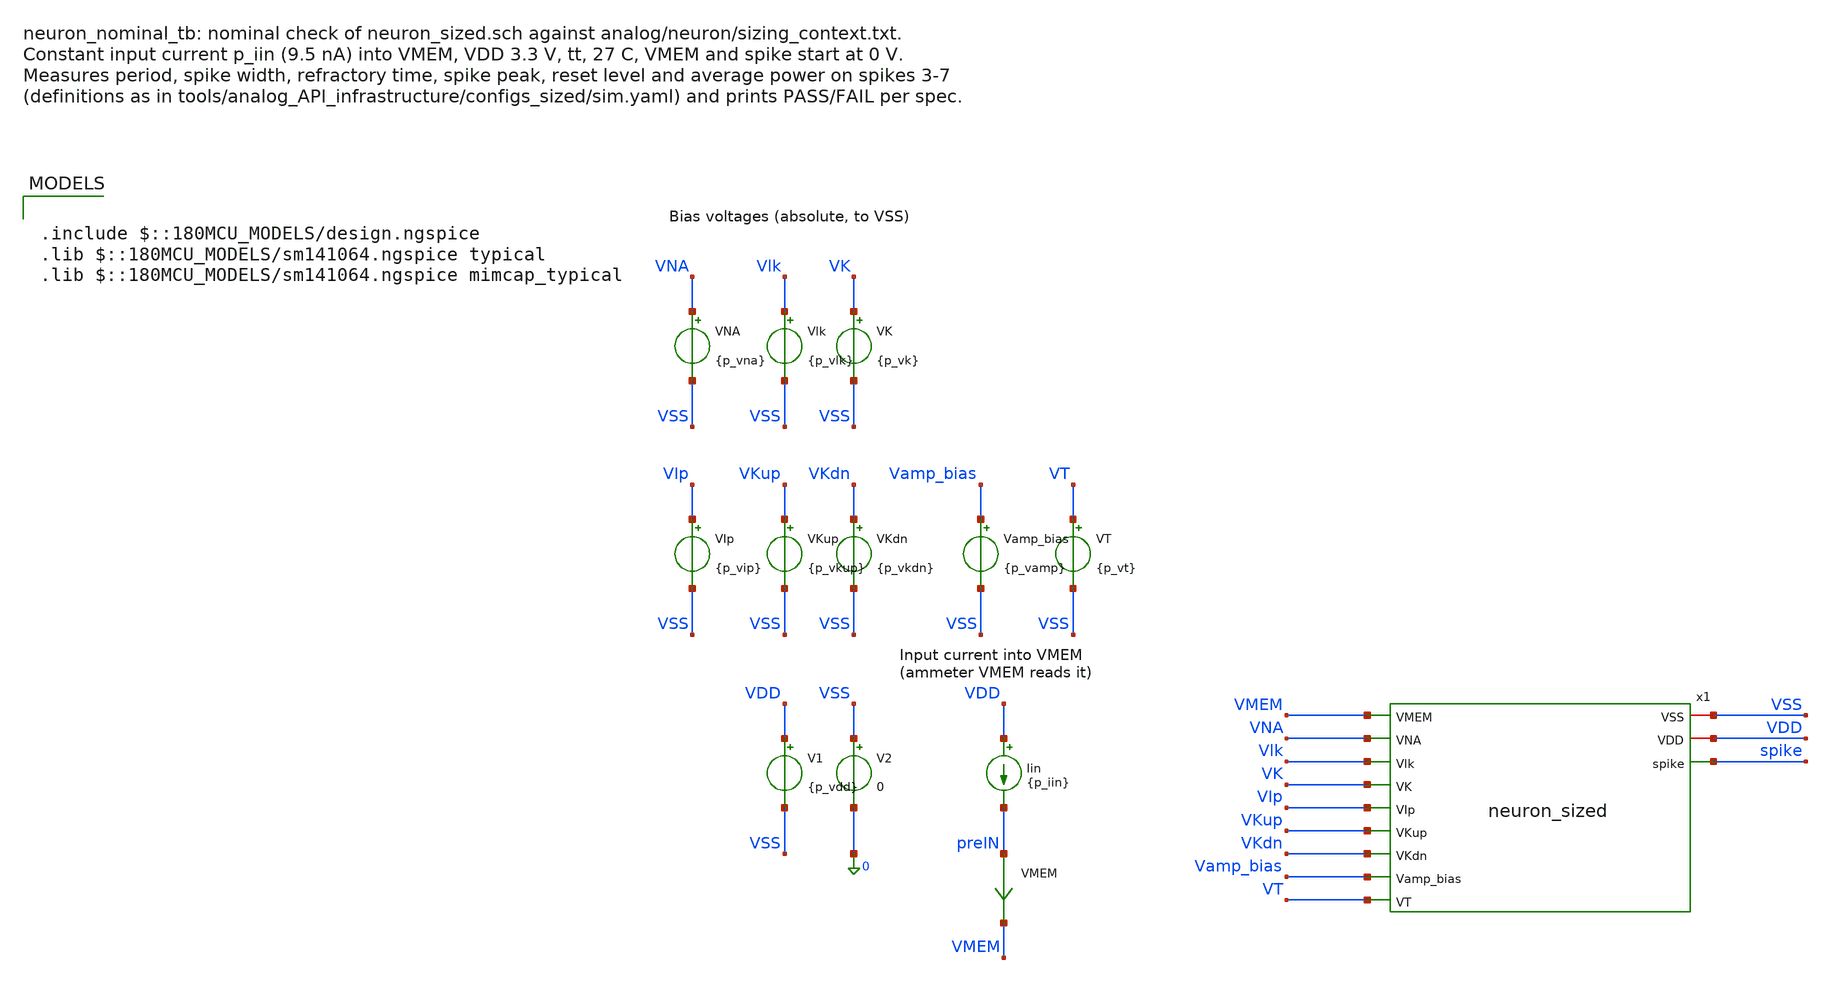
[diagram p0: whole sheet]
** sch_path: analog/testbenches/neuron/neuron_nominal_tb.sch
**.subckt neuron_nominal_tb
V1 VDD VSS {p_vdd}
V2 VSS 0 0
Iin VDD preIN {p_iin}
VMEM preIN VMEM 0
.save i(vmem)
x1 VSS VDD VMEM VNA Vlk VK VIp VKup VKdn Vamp_bias VT spike neuron_sized
Vlk Vlk VSS {p_vlk}
VK VK VSS {p_vk}
VNA VNA VSS {p_vna}
VKup VKup VSS {p_vkup}
VKdn VKdn VSS {p_vkdn}
VIp VIp VSS {p_vip}
VT VT VSS {p_vt}
Vamp_bias Vamp_bias VSS {p_vamp}
**** begin user architecture code

.include $::180MCU_MODELS/design.ngspice
.lib $::180MCU_MODELS/sm141064.ngspice typical
.lib $::180MCU_MODELS/sm141064.ngspice mimcap_typical



* Operating point of neuron_sized (analog/Analog_AI_Documentation.md entry 42).
* Parameters start with p_ because a .param named like a net (VT, Vlk, ...) can
* rename that net on the instance line (see mixed/README.md, Pitfalls).
.param p_vdd=3.3 p_iin=9.5n p_tstop=1.8m
.param p_vlk=0.425 p_vamp=0.535 p_vip=0.573 p_vna=1.93 p_vkup=2.35 p_vk=1.22 p_vkdn=0.588 p_vt=1.66
.csparam vdd_c={p_vdd}
.csparam tstop_c={p_tstop}
.ic v(VMEM)=0 v(spike)=0
.control
  save v(spike) v(VMEM) i(V1) i(VMEM)
  tran 20n $&tstop_c 0 20n uic

  * Spike edges at VDD/2. Spikes 1-2 start from the initial condition, so
  * everything is measured from spike 3 on. A failed measurement keeps -1.
  let vsw = vdd_c/2
  let t3 = -1
  let t4 = -1
  let t7 = -1
  let tf3 = -1
  let trst = -1
  let trel = -1
  meas tran t3 when v(spike)=$&vsw rise=3
  meas tran t4 when v(spike)=$&vsw rise=4
  meas tran t7 when v(spike)=$&vsw rise=7
  meas tran tf3 when v(spike)=$&vsw fall=3

  let nfail = 0
  if t7 < 0
    echo
    echo neuron_nominal_tb: FAIL, fewer than 7 spikes in $&tstop_c s, nothing measured
    echo RES fired7=0
  else
    echo RES fired7=1

    * period: mean spike-to-spike time over spikes 3-7
    let period = (t7 - t3)/4
    * t_spike: time v(spike) stays above VDD/2, spike 3
    let t_spike = tf3 - t3
    * v_spike_max / v_reset: highest spike and lowest VMEM from spike 3 to spike 4
    meas tran v_spike_max max v(spike) from=$&t3 to=$&t4
    meas tran v_reset min v(VMEM) from=$&t3 to=$&t4
    * t_refr: end of reset (VMEM falls below 10 % VDD) until VMEM is free again
    * (rises 10 mV above v_reset). t_refr_post counts from the spike's falling edge.
    let v10 = 0.1*vdd_c
    let vrel = v_reset + 0.01
    meas tran trst when v(VMEM)=$&v10 fall=1 td=$&t3
    meas tran trel when v(VMEM)=$&vrel rise=1 td=$&tf3
    let t_refr = trel - trst
    let t_refr_post = trel - tf3
    * p_avg: supply power over spikes 3-7, including the input current (fed from VDD)
    meas tran i_avg avg i(V1) from=$&t3 to=$&t7
    let p_avg = -i_avg*vdd_c
    meas tran i_in avg i(VMEM) from=$&t3 to=$&t7

    echo RES period=$&period
    echo RES t_spike=$&t_spike
    echo RES t_refr=$&t_refr
    echo RES t_refr_post=$&t_refr_post
    echo RES v_spike_max=$&v_spike_max
    echo RES v_reset=$&v_reset
    echo RES p_avg=$&p_avg
    echo RES i_in=$&i_in

    * Targets from analog/neuron/sizing_context.txt
    let x = period*1e6
    if (period >= 190e-6) & (period <= 210e-6)
      echo CHECK period       $&x us     target 190 to 210 us   PASS
    else
      echo CHECK period       $&x us     target 190 to 210 us   FAIL
      let nfail = nfail + 1
    end
    let x = t_spike*1e6
    if (t_spike >= 9e-6) & (t_spike <= 11e-6)
      echo CHECK t_spike      $&x us     target 9 to 11 us      PASS
    else
      echo CHECK t_spike      $&x us     target 9 to 11 us      FAIL
      let nfail = nfail + 1
    end
    let x = t_refr*1e6
    if (t_refr >= 12e-6) & (t_refr <= 15e-6)
      echo CHECK t_refr       $&x us     target 12 to 15 us     PASS
    else
      echo CHECK t_refr       $&x us     target 12 to 15 us     FAIL
      let nfail = nfail + 1
    end
    if v_spike_max >= 2.97
      echo CHECK v_spike_max  $&v_spike_max V      target >= 2.97 V       PASS
    else
      echo CHECK v_spike_max  $&v_spike_max V      target >= 2.97 V       FAIL
      let nfail = nfail + 1
    end
    let x = v_reset*1e3
    if v_reset <= 0.05
      echo CHECK v_reset      $&x mV     target <= 50 mV        PASS
    else
      echo CHECK v_reset      $&x mV     target <= 50 mV        FAIL
      let nfail = nfail + 1
    end
    let x = p_avg*1e6
    if p_avg <= 1e-6
      echo CHECK p_avg        $&x uW     target <= 1 uW         PASS
    else
      echo CHECK p_avg        $&x uW     target <= 1 uW         FAIL
      let nfail = nfail + 1
    end
    echo RES n_fail=$&nfail
    if nfail = 0
      echo neuron_nominal_tb: PASS, all 6 simulated specs met
    else
      echo neuron_nominal_tb: FAIL, $&nfail specs not met
    end
  end

  * Waveforms (time, VMEM, spike). From the GUI they go to this testbench's
  * folder; in batch mode (runner scripts) to the run's own folder, so that
  * parallel runs don't overwrite each other.
  set wr_singlescale
  set wr_vecnames
  if $?batchmode = 0
    wrdata /foss/designs/engn2912e-project/analog/testbenches/neuron/results/neuron_nominal_tb.txt
+ v(VMEM) v(spike)
  else
    wrdata neuron_nominal_tb.txt v(VMEM) v(spike)
  end
  if $?batchmode = 0
    plot v(VMEM) v(spike) title 'neuron_nominal_tb: membrane and spike' xlabel 't (s)' ylabel 'V'
  end
.endc


**** end user architecture code
**.ends
.end
